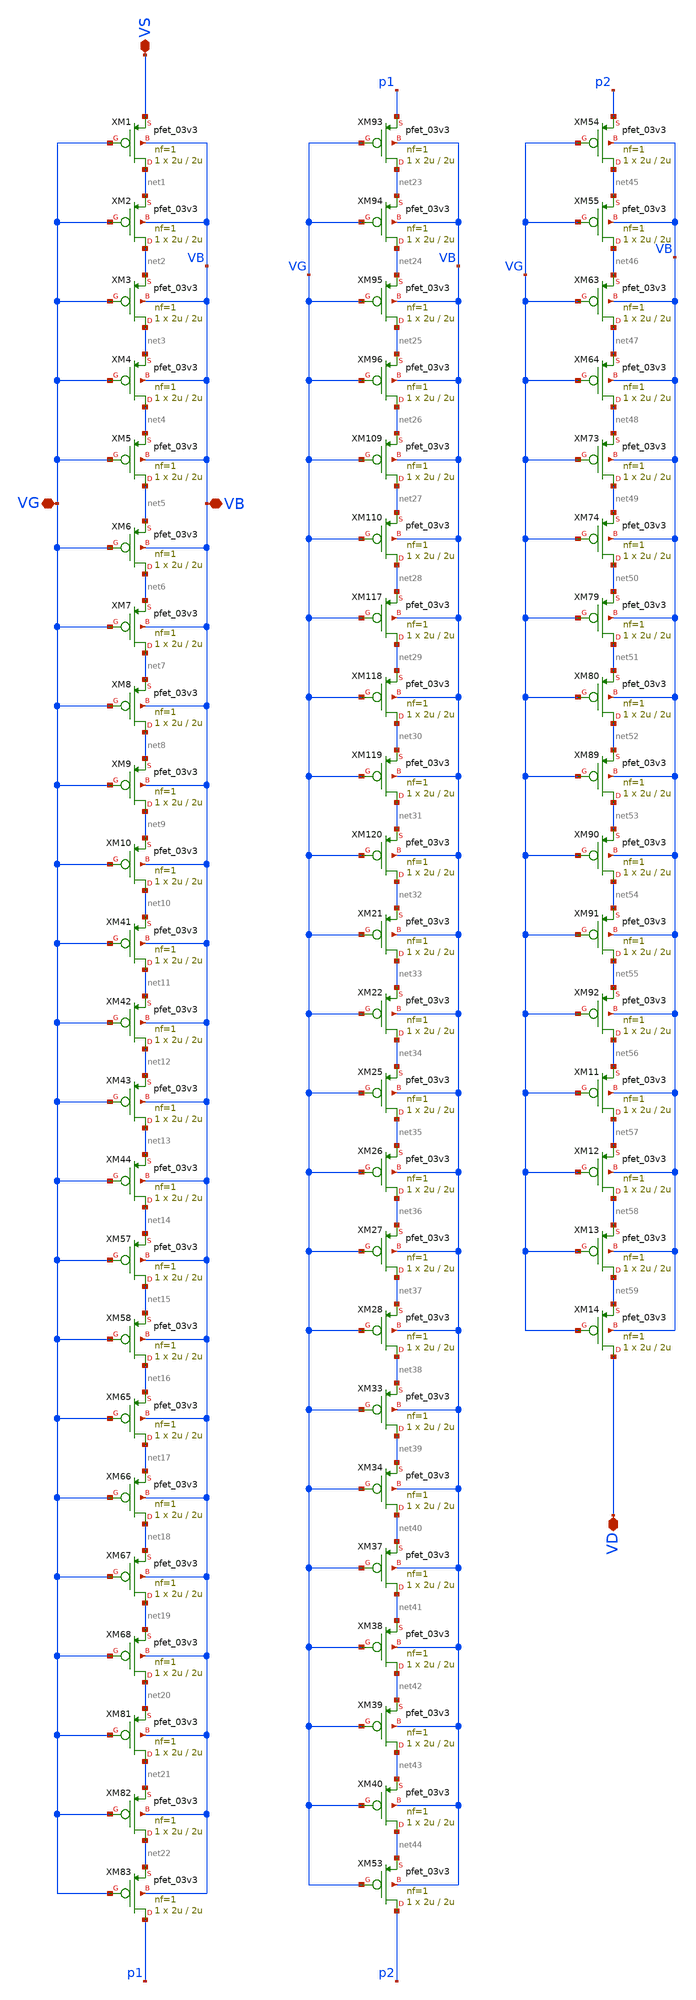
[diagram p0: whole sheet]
** sch_path: Voltage_Reference/symbols/PMOS_association_4u_10u.sch
**.subckt PMOS_association_4u_10u VD VB VG VS
*.iopin VD
*.iopin VB
*.iopin VG
*.iopin VS
XM1 net1 VG VS VB pfet_03v3 L=2u W=2u nf=1 ad='int((nf+1)/2) * W/nf * 0.18u' as='int((nf+2)/2) * W/nf * 0.18u'
+ pd='2*int((nf+1)/2) * (W/nf + 0.18u)' ps='2*int((nf+2)/2) * (W/nf + 0.18u)' nrd='0.18u / W' nrs='0.18u / W'
+ sa=0 sb=0 sd=0 m=1
XM2 net2 VG net1 VB pfet_03v3 L=2u W=2u nf=1 ad='int((nf+1)/2) * W/nf * 0.18u' as='int((nf+2)/2) * W/nf * 0.18u'
+ pd='2*int((nf+1)/2) * (W/nf + 0.18u)' ps='2*int((nf+2)/2) * (W/nf + 0.18u)' nrd='0.18u / W' nrs='0.18u / W'
+ sa=0 sb=0 sd=0 m=1
XM3 net3 VG net2 VB pfet_03v3 L=2u W=2u nf=1 ad='int((nf+1)/2) * W/nf * 0.18u' as='int((nf+2)/2) * W/nf * 0.18u'
+ pd='2*int((nf+1)/2) * (W/nf + 0.18u)' ps='2*int((nf+2)/2) * (W/nf + 0.18u)' nrd='0.18u / W' nrs='0.18u / W'
+ sa=0 sb=0 sd=0 m=1
XM4 net4 VG net3 VB pfet_03v3 L=2u W=2u nf=1 ad='int((nf+1)/2) * W/nf * 0.18u' as='int((nf+2)/2) * W/nf * 0.18u'
+ pd='2*int((nf+1)/2) * (W/nf + 0.18u)' ps='2*int((nf+2)/2) * (W/nf + 0.18u)' nrd='0.18u / W' nrs='0.18u / W'
+ sa=0 sb=0 sd=0 m=1
XM5 net5 VG net4 VB pfet_03v3 L=2u W=2u nf=1 ad='int((nf+1)/2) * W/nf * 0.18u' as='int((nf+2)/2) * W/nf * 0.18u'
+ pd='2*int((nf+1)/2) * (W/nf + 0.18u)' ps='2*int((nf+2)/2) * (W/nf + 0.18u)' nrd='0.18u / W' nrs='0.18u / W'
+ sa=0 sb=0 sd=0 m=1
XM6 net6 VG net5 VB pfet_03v3 L=2u W=2u nf=1 ad='int((nf+1)/2) * W/nf * 0.18u' as='int((nf+2)/2) * W/nf * 0.18u'
+ pd='2*int((nf+1)/2) * (W/nf + 0.18u)' ps='2*int((nf+2)/2) * (W/nf + 0.18u)' nrd='0.18u / W' nrs='0.18u / W'
+ sa=0 sb=0 sd=0 m=1
XM7 net7 VG net6 VB pfet_03v3 L=2u W=2u nf=1 ad='int((nf+1)/2) * W/nf * 0.18u' as='int((nf+2)/2) * W/nf * 0.18u'
+ pd='2*int((nf+1)/2) * (W/nf + 0.18u)' ps='2*int((nf+2)/2) * (W/nf + 0.18u)' nrd='0.18u / W' nrs='0.18u / W'
+ sa=0 sb=0 sd=0 m=1
XM8 net8 VG net7 VB pfet_03v3 L=2u W=2u nf=1 ad='int((nf+1)/2) * W/nf * 0.18u' as='int((nf+2)/2) * W/nf * 0.18u'
+ pd='2*int((nf+1)/2) * (W/nf + 0.18u)' ps='2*int((nf+2)/2) * (W/nf + 0.18u)' nrd='0.18u / W' nrs='0.18u / W'
+ sa=0 sb=0 sd=0 m=1
XM9 net9 VG net8 VB pfet_03v3 L=2u W=2u nf=1 ad='int((nf+1)/2) * W/nf * 0.18u' as='int((nf+2)/2) * W/nf * 0.18u'
+ pd='2*int((nf+1)/2) * (W/nf + 0.18u)' ps='2*int((nf+2)/2) * (W/nf + 0.18u)' nrd='0.18u / W' nrs='0.18u / W'
+ sa=0 sb=0 sd=0 m=1
XM10 net10 VG net9 VB pfet_03v3 L=2u W=2u nf=1 ad='int((nf+1)/2) * W/nf * 0.18u' as='int((nf+2)/2) * W/nf * 0.18u'
+ pd='2*int((nf+1)/2) * (W/nf + 0.18u)' ps='2*int((nf+2)/2) * (W/nf + 0.18u)' nrd='0.18u / W' nrs='0.18u / W'
+ sa=0 sb=0 sd=0 m=1
XM41 net11 VG net10 VB pfet_03v3 L=2u W=2u nf=1 ad='int((nf+1)/2) * W/nf * 0.18u' as='int((nf+2)/2) * W/nf * 0.18u'
+ pd='2*int((nf+1)/2) * (W/nf + 0.18u)' ps='2*int((nf+2)/2) * (W/nf + 0.18u)' nrd='0.18u / W' nrs='0.18u / W'
+ sa=0 sb=0 sd=0 m=1
XM42 net12 VG net11 VB pfet_03v3 L=2u W=2u nf=1 ad='int((nf+1)/2) * W/nf * 0.18u' as='int((nf+2)/2) * W/nf * 0.18u'
+ pd='2*int((nf+1)/2) * (W/nf + 0.18u)' ps='2*int((nf+2)/2) * (W/nf + 0.18u)' nrd='0.18u / W' nrs='0.18u / W'
+ sa=0 sb=0 sd=0 m=1
XM43 net13 VG net12 VB pfet_03v3 L=2u W=2u nf=1 ad='int((nf+1)/2) * W/nf * 0.18u' as='int((nf+2)/2) * W/nf * 0.18u'
+ pd='2*int((nf+1)/2) * (W/nf + 0.18u)' ps='2*int((nf+2)/2) * (W/nf + 0.18u)' nrd='0.18u / W' nrs='0.18u / W'
+ sa=0 sb=0 sd=0 m=1
XM44 net14 VG net13 VB pfet_03v3 L=2u W=2u nf=1 ad='int((nf+1)/2) * W/nf * 0.18u' as='int((nf+2)/2) * W/nf * 0.18u'
+ pd='2*int((nf+1)/2) * (W/nf + 0.18u)' ps='2*int((nf+2)/2) * (W/nf + 0.18u)' nrd='0.18u / W' nrs='0.18u / W'
+ sa=0 sb=0 sd=0 m=1
XM57 net15 VG net14 VB pfet_03v3 L=2u W=2u nf=1 ad='int((nf+1)/2) * W/nf * 0.18u' as='int((nf+2)/2) * W/nf * 0.18u'
+ pd='2*int((nf+1)/2) * (W/nf + 0.18u)' ps='2*int((nf+2)/2) * (W/nf + 0.18u)' nrd='0.18u / W' nrs='0.18u / W'
+ sa=0 sb=0 sd=0 m=1
XM58 net16 VG net15 VB pfet_03v3 L=2u W=2u nf=1 ad='int((nf+1)/2) * W/nf * 0.18u' as='int((nf+2)/2) * W/nf * 0.18u'
+ pd='2*int((nf+1)/2) * (W/nf + 0.18u)' ps='2*int((nf+2)/2) * (W/nf + 0.18u)' nrd='0.18u / W' nrs='0.18u / W'
+ sa=0 sb=0 sd=0 m=1
XM65 net17 VG net16 VB pfet_03v3 L=2u W=2u nf=1 ad='int((nf+1)/2) * W/nf * 0.18u' as='int((nf+2)/2) * W/nf * 0.18u'
+ pd='2*int((nf+1)/2) * (W/nf + 0.18u)' ps='2*int((nf+2)/2) * (W/nf + 0.18u)' nrd='0.18u / W' nrs='0.18u / W'
+ sa=0 sb=0 sd=0 m=1
XM66 net18 VG net17 VB pfet_03v3 L=2u W=2u nf=1 ad='int((nf+1)/2) * W/nf * 0.18u' as='int((nf+2)/2) * W/nf * 0.18u'
+ pd='2*int((nf+1)/2) * (W/nf + 0.18u)' ps='2*int((nf+2)/2) * (W/nf + 0.18u)' nrd='0.18u / W' nrs='0.18u / W'
+ sa=0 sb=0 sd=0 m=1
XM67 net19 VG net18 VB pfet_03v3 L=2u W=2u nf=1 ad='int((nf+1)/2) * W/nf * 0.18u' as='int((nf+2)/2) * W/nf * 0.18u'
+ pd='2*int((nf+1)/2) * (W/nf + 0.18u)' ps='2*int((nf+2)/2) * (W/nf + 0.18u)' nrd='0.18u / W' nrs='0.18u / W'
+ sa=0 sb=0 sd=0 m=1
XM68 net20 VG net19 VB pfet_03v3 L=2u W=2u nf=1 ad='int((nf+1)/2) * W/nf * 0.18u' as='int((nf+2)/2) * W/nf * 0.18u'
+ pd='2*int((nf+1)/2) * (W/nf + 0.18u)' ps='2*int((nf+2)/2) * (W/nf + 0.18u)' nrd='0.18u / W' nrs='0.18u / W'
+ sa=0 sb=0 sd=0 m=1
XM81 net21 VG net20 VB pfet_03v3 L=2u W=2u nf=1 ad='int((nf+1)/2) * W/nf * 0.18u' as='int((nf+2)/2) * W/nf * 0.18u'
+ pd='2*int((nf+1)/2) * (W/nf + 0.18u)' ps='2*int((nf+2)/2) * (W/nf + 0.18u)' nrd='0.18u / W' nrs='0.18u / W'
+ sa=0 sb=0 sd=0 m=1
XM82 net22 VG net21 VB pfet_03v3 L=2u W=2u nf=1 ad='int((nf+1)/2) * W/nf * 0.18u' as='int((nf+2)/2) * W/nf * 0.18u'
+ pd='2*int((nf+1)/2) * (W/nf + 0.18u)' ps='2*int((nf+2)/2) * (W/nf + 0.18u)' nrd='0.18u / W' nrs='0.18u / W'
+ sa=0 sb=0 sd=0 m=1
XM83 p1 VG net22 VB pfet_03v3 L=2u W=2u nf=1 ad='int((nf+1)/2) * W/nf * 0.18u' as='int((nf+2)/2) * W/nf * 0.18u'
+ pd='2*int((nf+1)/2) * (W/nf + 0.18u)' ps='2*int((nf+2)/2) * (W/nf + 0.18u)' nrd='0.18u / W' nrs='0.18u / W'
+ sa=0 sb=0 sd=0 m=1
XM93 net23 VG p1 VB pfet_03v3 L=2u W=2u nf=1 ad='int((nf+1)/2) * W/nf * 0.18u' as='int((nf+2)/2) * W/nf * 0.18u'
+ pd='2*int((nf+1)/2) * (W/nf + 0.18u)' ps='2*int((nf+2)/2) * (W/nf + 0.18u)' nrd='0.18u / W' nrs='0.18u / W'
+ sa=0 sb=0 sd=0 m=1
XM94 net24 VG net23 VB pfet_03v3 L=2u W=2u nf=1 ad='int((nf+1)/2) * W/nf * 0.18u' as='int((nf+2)/2) * W/nf * 0.18u'
+ pd='2*int((nf+1)/2) * (W/nf + 0.18u)' ps='2*int((nf+2)/2) * (W/nf + 0.18u)' nrd='0.18u / W' nrs='0.18u / W'
+ sa=0 sb=0 sd=0 m=1
XM95 net25 VG net24 VB pfet_03v3 L=2u W=2u nf=1 ad='int((nf+1)/2) * W/nf * 0.18u' as='int((nf+2)/2) * W/nf * 0.18u'
+ pd='2*int((nf+1)/2) * (W/nf + 0.18u)' ps='2*int((nf+2)/2) * (W/nf + 0.18u)' nrd='0.18u / W' nrs='0.18u / W'
+ sa=0 sb=0 sd=0 m=1
XM96 net26 VG net25 VB pfet_03v3 L=2u W=2u nf=1 ad='int((nf+1)/2) * W/nf * 0.18u' as='int((nf+2)/2) * W/nf * 0.18u'
+ pd='2*int((nf+1)/2) * (W/nf + 0.18u)' ps='2*int((nf+2)/2) * (W/nf + 0.18u)' nrd='0.18u / W' nrs='0.18u / W'
+ sa=0 sb=0 sd=0 m=1
XM109 net27 VG net26 VB pfet_03v3 L=2u W=2u nf=1 ad='int((nf+1)/2) * W/nf * 0.18u' as='int((nf+2)/2) * W/nf * 0.18u'
+ pd='2*int((nf+1)/2) * (W/nf + 0.18u)' ps='2*int((nf+2)/2) * (W/nf + 0.18u)' nrd='0.18u / W' nrs='0.18u / W'
+ sa=0 sb=0 sd=0 m=1
XM110 net28 VG net27 VB pfet_03v3 L=2u W=2u nf=1 ad='int((nf+1)/2) * W/nf * 0.18u' as='int((nf+2)/2) * W/nf * 0.18u'
+ pd='2*int((nf+1)/2) * (W/nf + 0.18u)' ps='2*int((nf+2)/2) * (W/nf + 0.18u)' nrd='0.18u / W' nrs='0.18u / W'
+ sa=0 sb=0 sd=0 m=1
XM117 net29 VG net28 VB pfet_03v3 L=2u W=2u nf=1 ad='int((nf+1)/2) * W/nf * 0.18u' as='int((nf+2)/2) * W/nf * 0.18u'
+ pd='2*int((nf+1)/2) * (W/nf + 0.18u)' ps='2*int((nf+2)/2) * (W/nf + 0.18u)' nrd='0.18u / W' nrs='0.18u / W'
+ sa=0 sb=0 sd=0 m=1
XM118 net30 VG net29 VB pfet_03v3 L=2u W=2u nf=1 ad='int((nf+1)/2) * W/nf * 0.18u' as='int((nf+2)/2) * W/nf * 0.18u'
+ pd='2*int((nf+1)/2) * (W/nf + 0.18u)' ps='2*int((nf+2)/2) * (W/nf + 0.18u)' nrd='0.18u / W' nrs='0.18u / W'
+ sa=0 sb=0 sd=0 m=1
XM119 net31 VG net30 VB pfet_03v3 L=2u W=2u nf=1 ad='int((nf+1)/2) * W/nf * 0.18u' as='int((nf+2)/2) * W/nf * 0.18u'
+ pd='2*int((nf+1)/2) * (W/nf + 0.18u)' ps='2*int((nf+2)/2) * (W/nf + 0.18u)' nrd='0.18u / W' nrs='0.18u / W'
+ sa=0 sb=0 sd=0 m=1
XM120 net32 VG net31 VB pfet_03v3 L=2u W=2u nf=1 ad='int((nf+1)/2) * W/nf * 0.18u' as='int((nf+2)/2) * W/nf * 0.18u'
+ pd='2*int((nf+1)/2) * (W/nf + 0.18u)' ps='2*int((nf+2)/2) * (W/nf + 0.18u)' nrd='0.18u / W' nrs='0.18u / W'
+ sa=0 sb=0 sd=0 m=1
XM21 net33 VG net32 VB pfet_03v3 L=2u W=2u nf=1 ad='int((nf+1)/2) * W/nf * 0.18u' as='int((nf+2)/2) * W/nf * 0.18u'
+ pd='2*int((nf+1)/2) * (W/nf + 0.18u)' ps='2*int((nf+2)/2) * (W/nf + 0.18u)' nrd='0.18u / W' nrs='0.18u / W'
+ sa=0 sb=0 sd=0 m=1
XM22 net34 VG net33 VB pfet_03v3 L=2u W=2u nf=1 ad='int((nf+1)/2) * W/nf * 0.18u' as='int((nf+2)/2) * W/nf * 0.18u'
+ pd='2*int((nf+1)/2) * (W/nf + 0.18u)' ps='2*int((nf+2)/2) * (W/nf + 0.18u)' nrd='0.18u / W' nrs='0.18u / W'
+ sa=0 sb=0 sd=0 m=1
XM25 net35 VG net34 VB pfet_03v3 L=2u W=2u nf=1 ad='int((nf+1)/2) * W/nf * 0.18u' as='int((nf+2)/2) * W/nf * 0.18u'
+ pd='2*int((nf+1)/2) * (W/nf + 0.18u)' ps='2*int((nf+2)/2) * (W/nf + 0.18u)' nrd='0.18u / W' nrs='0.18u / W'
+ sa=0 sb=0 sd=0 m=1
XM26 net36 VG net35 VB pfet_03v3 L=2u W=2u nf=1 ad='int((nf+1)/2) * W/nf * 0.18u' as='int((nf+2)/2) * W/nf * 0.18u'
+ pd='2*int((nf+1)/2) * (W/nf + 0.18u)' ps='2*int((nf+2)/2) * (W/nf + 0.18u)' nrd='0.18u / W' nrs='0.18u / W'
+ sa=0 sb=0 sd=0 m=1
XM27 net37 VG net36 VB pfet_03v3 L=2u W=2u nf=1 ad='int((nf+1)/2) * W/nf * 0.18u' as='int((nf+2)/2) * W/nf * 0.18u'
+ pd='2*int((nf+1)/2) * (W/nf + 0.18u)' ps='2*int((nf+2)/2) * (W/nf + 0.18u)' nrd='0.18u / W' nrs='0.18u / W'
+ sa=0 sb=0 sd=0 m=1
XM28 net38 VG net37 VB pfet_03v3 L=2u W=2u nf=1 ad='int((nf+1)/2) * W/nf * 0.18u' as='int((nf+2)/2) * W/nf * 0.18u'
+ pd='2*int((nf+1)/2) * (W/nf + 0.18u)' ps='2*int((nf+2)/2) * (W/nf + 0.18u)' nrd='0.18u / W' nrs='0.18u / W'
+ sa=0 sb=0 sd=0 m=1
XM33 net39 VG net38 VB pfet_03v3 L=2u W=2u nf=1 ad='int((nf+1)/2) * W/nf * 0.18u' as='int((nf+2)/2) * W/nf * 0.18u'
+ pd='2*int((nf+1)/2) * (W/nf + 0.18u)' ps='2*int((nf+2)/2) * (W/nf + 0.18u)' nrd='0.18u / W' nrs='0.18u / W'
+ sa=0 sb=0 sd=0 m=1
XM34 net40 VG net39 VB pfet_03v3 L=2u W=2u nf=1 ad='int((nf+1)/2) * W/nf * 0.18u' as='int((nf+2)/2) * W/nf * 0.18u'
+ pd='2*int((nf+1)/2) * (W/nf + 0.18u)' ps='2*int((nf+2)/2) * (W/nf + 0.18u)' nrd='0.18u / W' nrs='0.18u / W'
+ sa=0 sb=0 sd=0 m=1
XM37 net41 VG net40 VB pfet_03v3 L=2u W=2u nf=1 ad='int((nf+1)/2) * W/nf * 0.18u' as='int((nf+2)/2) * W/nf * 0.18u'
+ pd='2*int((nf+1)/2) * (W/nf + 0.18u)' ps='2*int((nf+2)/2) * (W/nf + 0.18u)' nrd='0.18u / W' nrs='0.18u / W'
+ sa=0 sb=0 sd=0 m=1
XM38 net42 VG net41 VB pfet_03v3 L=2u W=2u nf=1 ad='int((nf+1)/2) * W/nf * 0.18u' as='int((nf+2)/2) * W/nf * 0.18u'
+ pd='2*int((nf+1)/2) * (W/nf + 0.18u)' ps='2*int((nf+2)/2) * (W/nf + 0.18u)' nrd='0.18u / W' nrs='0.18u / W'
+ sa=0 sb=0 sd=0 m=1
XM39 net43 VG net42 VB pfet_03v3 L=2u W=2u nf=1 ad='int((nf+1)/2) * W/nf * 0.18u' as='int((nf+2)/2) * W/nf * 0.18u'
+ pd='2*int((nf+1)/2) * (W/nf + 0.18u)' ps='2*int((nf+2)/2) * (W/nf + 0.18u)' nrd='0.18u / W' nrs='0.18u / W'
+ sa=0 sb=0 sd=0 m=1
XM40 net44 VG net43 VB pfet_03v3 L=2u W=2u nf=1 ad='int((nf+1)/2) * W/nf * 0.18u' as='int((nf+2)/2) * W/nf * 0.18u'
+ pd='2*int((nf+1)/2) * (W/nf + 0.18u)' ps='2*int((nf+2)/2) * (W/nf + 0.18u)' nrd='0.18u / W' nrs='0.18u / W'
+ sa=0 sb=0 sd=0 m=1
XM53 p2 VG net44 VB pfet_03v3 L=2u W=2u nf=1 ad='int((nf+1)/2) * W/nf * 0.18u' as='int((nf+2)/2) * W/nf * 0.18u'
+ pd='2*int((nf+1)/2) * (W/nf + 0.18u)' ps='2*int((nf+2)/2) * (W/nf + 0.18u)' nrd='0.18u / W' nrs='0.18u / W'
+ sa=0 sb=0 sd=0 m=1
XM54 net45 VG p2 VB pfet_03v3 L=2u W=2u nf=1 ad='int((nf+1)/2) * W/nf * 0.18u' as='int((nf+2)/2) * W/nf * 0.18u'
+ pd='2*int((nf+1)/2) * (W/nf + 0.18u)' ps='2*int((nf+2)/2) * (W/nf + 0.18u)' nrd='0.18u / W' nrs='0.18u / W'
+ sa=0 sb=0 sd=0 m=1
XM55 net46 VG net45 VB pfet_03v3 L=2u W=2u nf=1 ad='int((nf+1)/2) * W/nf * 0.18u' as='int((nf+2)/2) * W/nf * 0.18u'
+ pd='2*int((nf+1)/2) * (W/nf + 0.18u)' ps='2*int((nf+2)/2) * (W/nf + 0.18u)' nrd='0.18u / W' nrs='0.18u / W'
+ sa=0 sb=0 sd=0 m=1
XM63 net47 VG net46 VB pfet_03v3 L=2u W=2u nf=1 ad='int((nf+1)/2) * W/nf * 0.18u' as='int((nf+2)/2) * W/nf * 0.18u'
+ pd='2*int((nf+1)/2) * (W/nf + 0.18u)' ps='2*int((nf+2)/2) * (W/nf + 0.18u)' nrd='0.18u / W' nrs='0.18u / W'
+ sa=0 sb=0 sd=0 m=1
XM64 net48 VG net47 VB pfet_03v3 L=2u W=2u nf=1 ad='int((nf+1)/2) * W/nf * 0.18u' as='int((nf+2)/2) * W/nf * 0.18u'
+ pd='2*int((nf+1)/2) * (W/nf + 0.18u)' ps='2*int((nf+2)/2) * (W/nf + 0.18u)' nrd='0.18u / W' nrs='0.18u / W'
+ sa=0 sb=0 sd=0 m=1
XM73 net49 VG net48 VB pfet_03v3 L=2u W=2u nf=1 ad='int((nf+1)/2) * W/nf * 0.18u' as='int((nf+2)/2) * W/nf * 0.18u'
+ pd='2*int((nf+1)/2) * (W/nf + 0.18u)' ps='2*int((nf+2)/2) * (W/nf + 0.18u)' nrd='0.18u / W' nrs='0.18u / W'
+ sa=0 sb=0 sd=0 m=1
XM74 net50 VG net49 VB pfet_03v3 L=2u W=2u nf=1 ad='int((nf+1)/2) * W/nf * 0.18u' as='int((nf+2)/2) * W/nf * 0.18u'
+ pd='2*int((nf+1)/2) * (W/nf + 0.18u)' ps='2*int((nf+2)/2) * (W/nf + 0.18u)' nrd='0.18u / W' nrs='0.18u / W'
+ sa=0 sb=0 sd=0 m=1
XM79 net51 VG net50 VB pfet_03v3 L=2u W=2u nf=1 ad='int((nf+1)/2) * W/nf * 0.18u' as='int((nf+2)/2) * W/nf * 0.18u'
+ pd='2*int((nf+1)/2) * (W/nf + 0.18u)' ps='2*int((nf+2)/2) * (W/nf + 0.18u)' nrd='0.18u / W' nrs='0.18u / W'
+ sa=0 sb=0 sd=0 m=1
XM80 net52 VG net51 VB pfet_03v3 L=2u W=2u nf=1 ad='int((nf+1)/2) * W/nf * 0.18u' as='int((nf+2)/2) * W/nf * 0.18u'
+ pd='2*int((nf+1)/2) * (W/nf + 0.18u)' ps='2*int((nf+2)/2) * (W/nf + 0.18u)' nrd='0.18u / W' nrs='0.18u / W'
+ sa=0 sb=0 sd=0 m=1
XM89 net53 VG net52 VB pfet_03v3 L=2u W=2u nf=1 ad='int((nf+1)/2) * W/nf * 0.18u' as='int((nf+2)/2) * W/nf * 0.18u'
+ pd='2*int((nf+1)/2) * (W/nf + 0.18u)' ps='2*int((nf+2)/2) * (W/nf + 0.18u)' nrd='0.18u / W' nrs='0.18u / W'
+ sa=0 sb=0 sd=0 m=1
XM90 net54 VG net53 VB pfet_03v3 L=2u W=2u nf=1 ad='int((nf+1)/2) * W/nf * 0.18u' as='int((nf+2)/2) * W/nf * 0.18u'
+ pd='2*int((nf+1)/2) * (W/nf + 0.18u)' ps='2*int((nf+2)/2) * (W/nf + 0.18u)' nrd='0.18u / W' nrs='0.18u / W'
+ sa=0 sb=0 sd=0 m=1
XM91 net55 VG net54 VB pfet_03v3 L=2u W=2u nf=1 ad='int((nf+1)/2) * W/nf * 0.18u' as='int((nf+2)/2) * W/nf * 0.18u'
+ pd='2*int((nf+1)/2) * (W/nf + 0.18u)' ps='2*int((nf+2)/2) * (W/nf + 0.18u)' nrd='0.18u / W' nrs='0.18u / W'
+ sa=0 sb=0 sd=0 m=1
XM92 net56 VG net55 VB pfet_03v3 L=2u W=2u nf=1 ad='int((nf+1)/2) * W/nf * 0.18u' as='int((nf+2)/2) * W/nf * 0.18u'
+ pd='2*int((nf+1)/2) * (W/nf + 0.18u)' ps='2*int((nf+2)/2) * (W/nf + 0.18u)' nrd='0.18u / W' nrs='0.18u / W'
+ sa=0 sb=0 sd=0 m=1
XM11 net57 VG net56 VB pfet_03v3 L=2u W=2u nf=1 ad='int((nf+1)/2) * W/nf * 0.18u' as='int((nf+2)/2) * W/nf * 0.18u'
+ pd='2*int((nf+1)/2) * (W/nf + 0.18u)' ps='2*int((nf+2)/2) * (W/nf + 0.18u)' nrd='0.18u / W' nrs='0.18u / W'
+ sa=0 sb=0 sd=0 m=1
XM12 net58 VG net57 VB pfet_03v3 L=2u W=2u nf=1 ad='int((nf+1)/2) * W/nf * 0.18u' as='int((nf+2)/2) * W/nf * 0.18u'
+ pd='2*int((nf+1)/2) * (W/nf + 0.18u)' ps='2*int((nf+2)/2) * (W/nf + 0.18u)' nrd='0.18u / W' nrs='0.18u / W'
+ sa=0 sb=0 sd=0 m=1
XM13 net59 VG net58 VB pfet_03v3 L=2u W=2u nf=1 ad='int((nf+1)/2) * W/nf * 0.18u' as='int((nf+2)/2) * W/nf * 0.18u'
+ pd='2*int((nf+1)/2) * (W/nf + 0.18u)' ps='2*int((nf+2)/2) * (W/nf + 0.18u)' nrd='0.18u / W' nrs='0.18u / W'
+ sa=0 sb=0 sd=0 m=1
XM14 VD VG net59 VB pfet_03v3 L=2u W=2u nf=1 ad='int((nf+1)/2) * W/nf * 0.18u' as='int((nf+2)/2) * W/nf * 0.18u'
+ pd='2*int((nf+1)/2) * (W/nf + 0.18u)' ps='2*int((nf+2)/2) * (W/nf + 0.18u)' nrd='0.18u / W' nrs='0.18u / W'
+ sa=0 sb=0 sd=0 m=1
**.ends
.end
